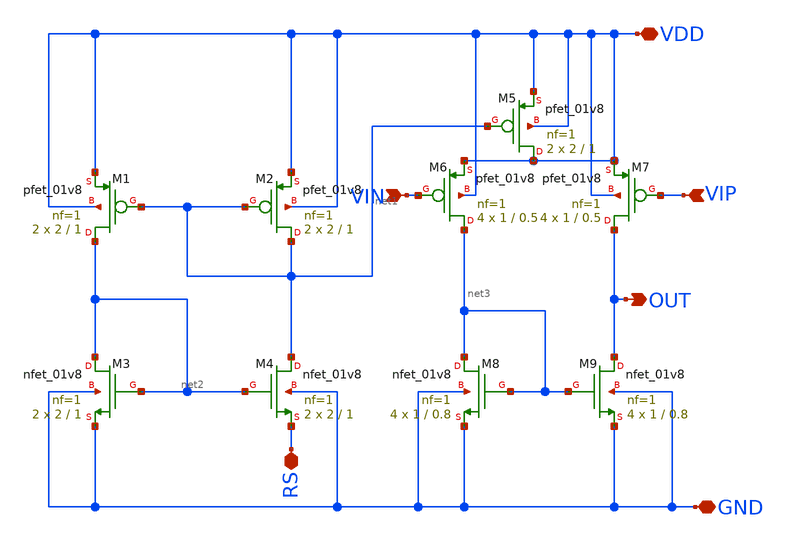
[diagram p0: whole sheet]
** sch_path: xschem/opamp.sch
**.subckt opamp VIN OUT VDD VIP GND RS
*.ipin VIN
*.opin OUT
*.iopin VDD
*.ipin VIP
*.iopin GND
*.iopin RS
XM4 net1 net2 RS GND sky130_fd_pr__nfet_01v8 L=1 W=2 nf=1 ad='int((nf+1)/2) * W/nf * 0.29' as='int((nf+2)/2) * W/nf * 0.29'
+ pd='2*int((nf+1)/2) * (W/nf + 0.29)' ps='2*int((nf+2)/2) * (W/nf + 0.29)' nrd='0.29 / W' nrs='0.29 / W'
+ sa=0 sb=0 sd=0 mult=2 m=2
XM2 net1 net1 VDD VDD sky130_fd_pr__pfet_01v8 L=1 W=2 nf=1 ad='int((nf+1)/2) * W/nf * 0.29' as='int((nf+2)/2) * W/nf * 0.29'
+ pd='2*int((nf+1)/2) * (W/nf + 0.29)' ps='2*int((nf+2)/2) * (W/nf + 0.29)' nrd='0.29 / W' nrs='0.29 / W'
+ sa=0 sb=0 sd=0 mult=2 m=2
XM1 net2 net1 VDD VDD sky130_fd_pr__pfet_01v8 L=1 W=2 nf=1 ad='int((nf+1)/2) * W/nf * 0.29' as='int((nf+2)/2) * W/nf * 0.29'
+ pd='2*int((nf+1)/2) * (W/nf + 0.29)' ps='2*int((nf+2)/2) * (W/nf + 0.29)' nrd='0.29 / W' nrs='0.29 / W'
+ sa=0 sb=0 sd=0 mult=2 m=2
XM3 net2 net2 GND GND sky130_fd_pr__nfet_01v8 L=1 W=2 nf=1 ad='int((nf+1)/2) * W/nf * 0.29' as='int((nf+2)/2) * W/nf * 0.29'
+ pd='2*int((nf+1)/2) * (W/nf + 0.29)' ps='2*int((nf+2)/2) * (W/nf + 0.29)' nrd='0.29 / W' nrs='0.29 / W'
+ sa=0 sb=0 sd=0 mult=2 m=2
XM8 net3 net3 GND GND sky130_fd_pr__nfet_01v8 L=0.8 W=1 nf=1 ad='int((nf+1)/2) * W/nf * 0.29' as='int((nf+2)/2) * W/nf * 0.29'
+ pd='2*int((nf+1)/2) * (W/nf + 0.29)' ps='2*int((nf+2)/2) * (W/nf + 0.29)' nrd='0.29 / W' nrs='0.29 / W'
+ sa=0 sb=0 sd=0 mult=4 m=4
XM9 OUT net3 GND GND sky130_fd_pr__nfet_01v8 L=0.8 W=1 nf=1 ad='int((nf+1)/2) * W/nf * 0.29' as='int((nf+2)/2) * W/nf * 0.29'
+ pd='2*int((nf+1)/2) * (W/nf + 0.29)' ps='2*int((nf+2)/2) * (W/nf + 0.29)' nrd='0.29 / W' nrs='0.29 / W'
+ sa=0 sb=0 sd=0 mult=4 m=4
XM7 OUT VIP VDD VDD sky130_fd_pr__pfet_01v8 L=0.5 W=1 nf=1 ad='int((nf+1)/2) * W/nf * 0.29' as='int((nf+2)/2) * W/nf * 0.29'
+ pd='2*int((nf+1)/2) * (W/nf + 0.29)' ps='2*int((nf+2)/2) * (W/nf + 0.29)' nrd='0.29 / W' nrs='0.29 / W'
+ sa=0 sb=0 sd=0 mult=4 m=4
XM6 net3 VIN VDD VDD sky130_fd_pr__pfet_01v8 L=0.5 W=1 nf=1 ad='int((nf+1)/2) * W/nf * 0.29' as='int((nf+2)/2) * W/nf * 0.29'
+ pd='2*int((nf+1)/2) * (W/nf + 0.29)' ps='2*int((nf+2)/2) * (W/nf + 0.29)' nrd='0.29 / W' nrs='0.29 / W'
+ sa=0 sb=0 sd=0 mult=4 m=4
XM5 VDD net1 VDD VDD sky130_fd_pr__pfet_01v8 L=1 W=2 nf=1 ad='int((nf+1)/2) * W/nf * 0.29' as='int((nf+2)/2) * W/nf * 0.29'
+ pd='2*int((nf+1)/2) * (W/nf + 0.29)' ps='2*int((nf+2)/2) * (W/nf + 0.29)' nrd='0.29 / W' nrs='0.29 / W'
+ sa=0 sb=0 sd=0 mult=2 m=2
**.ends
.end
